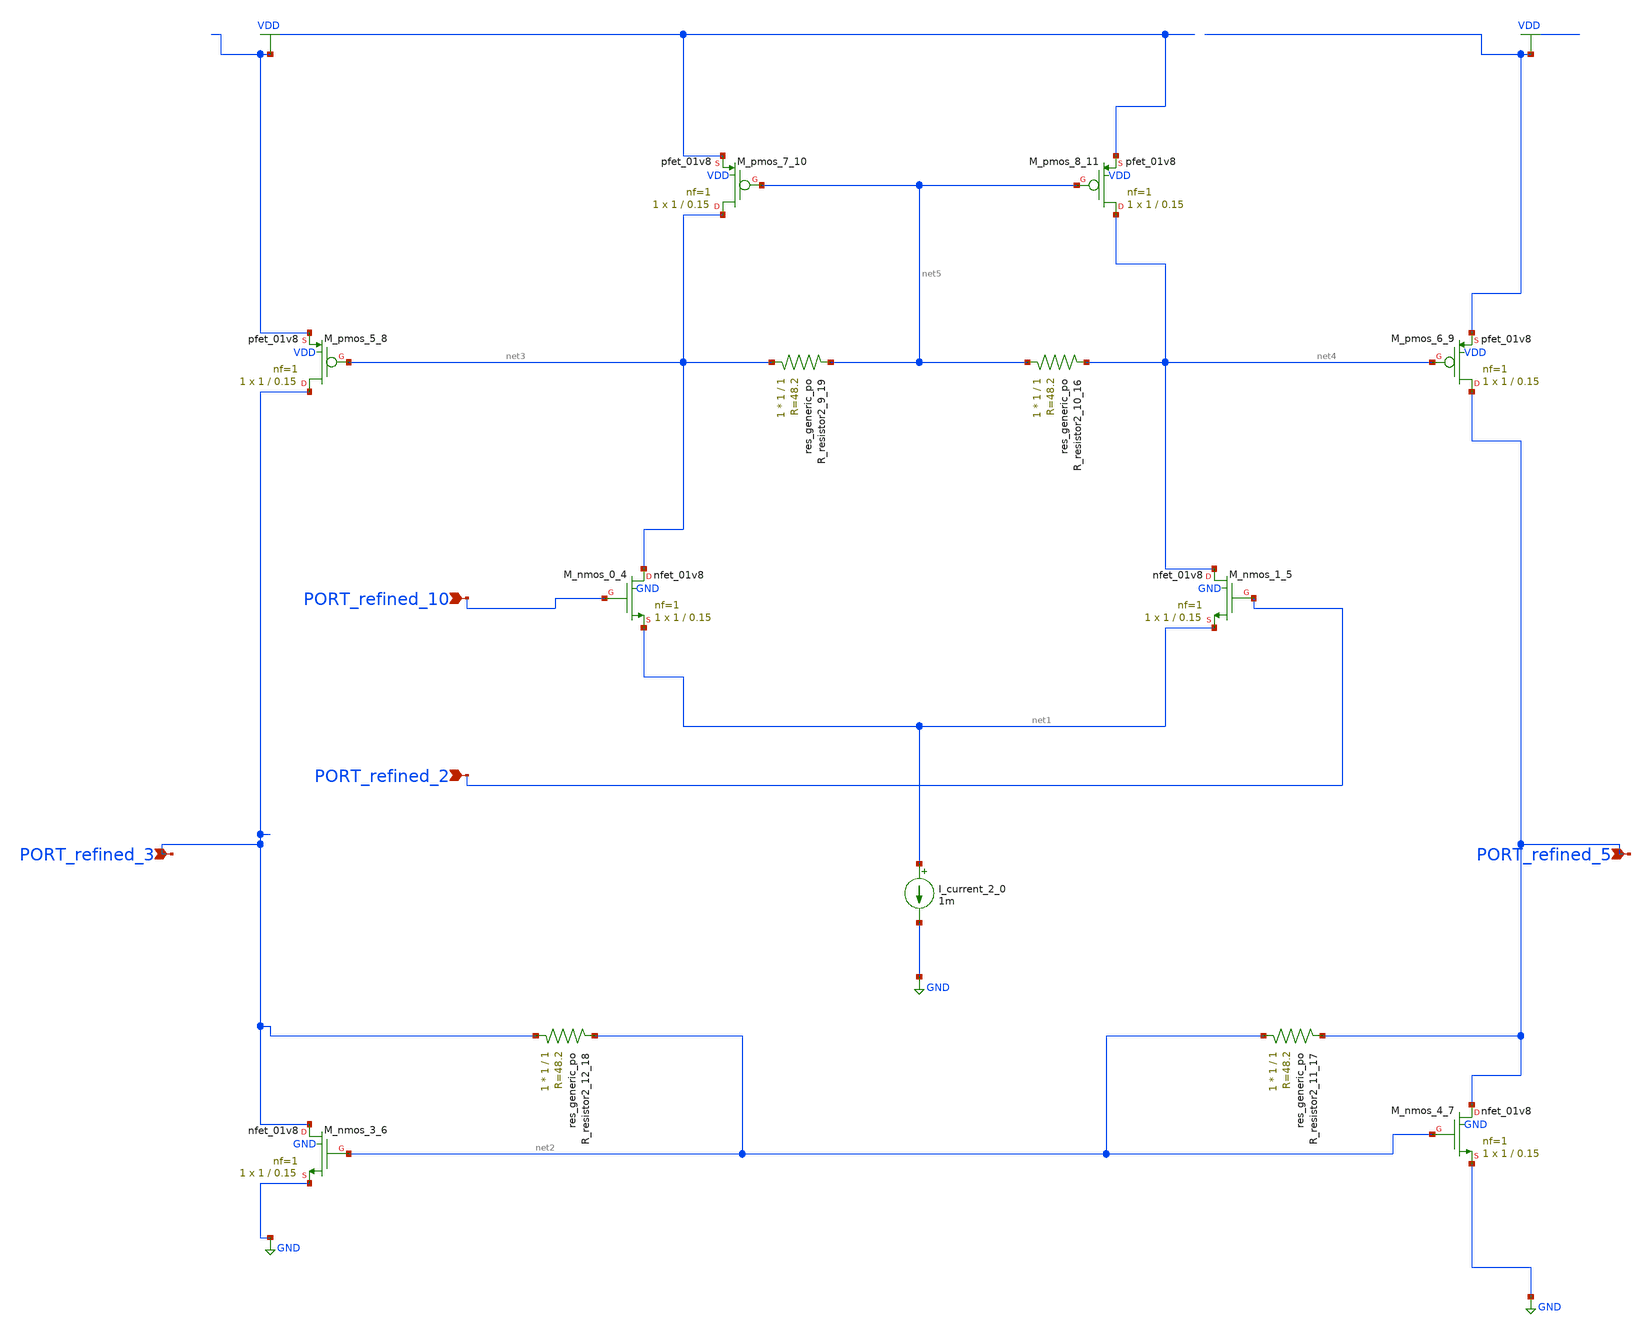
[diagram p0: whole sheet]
** sch_path: schematics/AMSNet/681.sch
**.subckt 681 PORT_refined_2 PORT_refined_5 PORT_refined_3 PORT_refined_10
*.ipin PORT_refined_2
*.ipin PORT_refined_5
*.ipin PORT_refined_3
*.ipin PORT_refined_10
I_current_2_0 net1 GND 1m
XM_nmos_0_4 net3 PORT_refined_10 net1 GND sky130_fd_pr__nfet_01v8 L=0.15 W=1 nf=1 ad='int((1 + 1)/2) * 1 / 1 * 0.29'
+ as='int((1 + 2)/2) * 1 / 1 * 0.29' pd='2*int((1 + 1)/2) * (1 / 1 + 0.29)' ps='2*int((1 + 2)/2) * (1 / 1 + 0.29)'
+ nrd='0.29 / 1 ' nrs='0.29 / 1 ' sa=0 sb=0 sd=0 mult=1 m=1
XM_nmos_1_5 net4 PORT_refined_2 net1 GND sky130_fd_pr__nfet_01v8 L=0.15 W=1 nf=1 ad='int((1 + 1)/2) * 1 / 1 * 0.29'
+ as='int((1 + 2)/2) * 1 / 1 * 0.29' pd='2*int((1 + 1)/2) * (1 / 1 + 0.29)' ps='2*int((1 + 2)/2) * (1 / 1 + 0.29)'
+ nrd='0.29 / 1 ' nrs='0.29 / 1 ' sa=0 sb=0 sd=0 mult=1 m=1
XM_nmos_3_6 PORT_refined_3 net2 GND GND sky130_fd_pr__nfet_01v8 L=0.15 W=1 nf=1 ad='int((1 + 1)/2) * 1 / 1 * 0.29'
+ as='int((1 + 2)/2) * 1 / 1 * 0.29' pd='2*int((1 + 1)/2) * (1 / 1 + 0.29)' ps='2*int((1 + 2)/2) * (1 / 1 + 0.29)'
+ nrd='0.29 / 1 ' nrs='0.29 / 1 ' sa=0 sb=0 sd=0 mult=1 m=1
XM_nmos_4_7 PORT_refined_5 net2 GND GND sky130_fd_pr__nfet_01v8 L=0.15 W=1 nf=1 ad='int((1 + 1)/2) * 1 / 1 * 0.29'
+ as='int((1 + 2)/2) * 1 / 1 * 0.29' pd='2*int((1 + 1)/2) * (1 / 1 + 0.29)' ps='2*int((1 + 2)/2) * (1 / 1 + 0.29)'
+ nrd='0.29 / 1 ' nrs='0.29 / 1 ' sa=0 sb=0 sd=0 mult=1 m=1
XM_pmos_5_8 PORT_refined_3 net3 VDD VDD sky130_fd_pr__pfet_01v8 L=0.15 W=1 nf=1 ad='int((1 + 1)/2) * 1 / 1 * 0.29'
+ as='int((1 + 2)/2) * 1 / 1 * 0.29' pd='2*int((1 + 1)/2) * (1 / 1 + 0.29)' ps='2*int((1 + 2)/2) * (1 / 1 + 0.29)'
+ nrd='0.29 / 1 ' nrs='0.29 / 1 ' sa=0 sb=0 sd=0 mult=1 m=1
XM_pmos_6_9 PORT_refined_5 net4 VDD VDD sky130_fd_pr__pfet_01v8 L=0.15 W=1 nf=1 ad='int((1 + 1)/2) * 1 / 1 * 0.29'
+ as='int((1 + 2)/2) * 1 / 1 * 0.29' pd='2*int((1 + 1)/2) * (1 / 1 + 0.29)' ps='2*int((1 + 2)/2) * (1 / 1 + 0.29)'
+ nrd='0.29 / 1 ' nrs='0.29 / 1 ' sa=0 sb=0 sd=0 mult=1 m=1
XM_pmos_7_10 net3 net5 VDD VDD sky130_fd_pr__pfet_01v8 L=0.15 W=1 nf=1 ad='int((1 + 1)/2) * 1 / 1 * 0.29'
+ as='int((1 + 2)/2) * 1 / 1 * 0.29' pd='2*int((1 + 1)/2) * (1 / 1 + 0.29)' ps='2*int((1 + 2)/2) * (1 / 1 + 0.29)'
+ nrd='0.29 / 1 ' nrs='0.29 / 1 ' sa=0 sb=0 sd=0 mult=1 m=1
XM_pmos_8_11 net4 net5 VDD VDD sky130_fd_pr__pfet_01v8 L=0.15 W=1 nf=1 ad='int((1 + 1)/2) * 1 / 1 * 0.29'
+ as='int((1 + 2)/2) * 1 / 1 * 0.29' pd='2*int((1 + 1)/2) * (1 / 1 + 0.29)' ps='2*int((1 + 2)/2) * (1 / 1 + 0.29)'
+ nrd='0.29 / 1 ' nrs='0.29 / 1 ' sa=0 sb=0 sd=0 mult=1 m=1
XR_resistor2_10_16 net5 net4 sky130_fd_pr__res_generic_po W=1 L=1 m=1
XR_resistor2_11_17 net2 PORT_refined_5 sky130_fd_pr__res_generic_po W=1 L=1 m=1
XR_resistor2_12_18 PORT_refined_3 net2 sky130_fd_pr__res_generic_po W=1 L=1 m=1
XR_resistor2_9_19 net3 net5 sky130_fd_pr__res_generic_po W=1 L=1 m=1
**.ends
.GLOBAL GND
.GLOBAL VDD
.end
